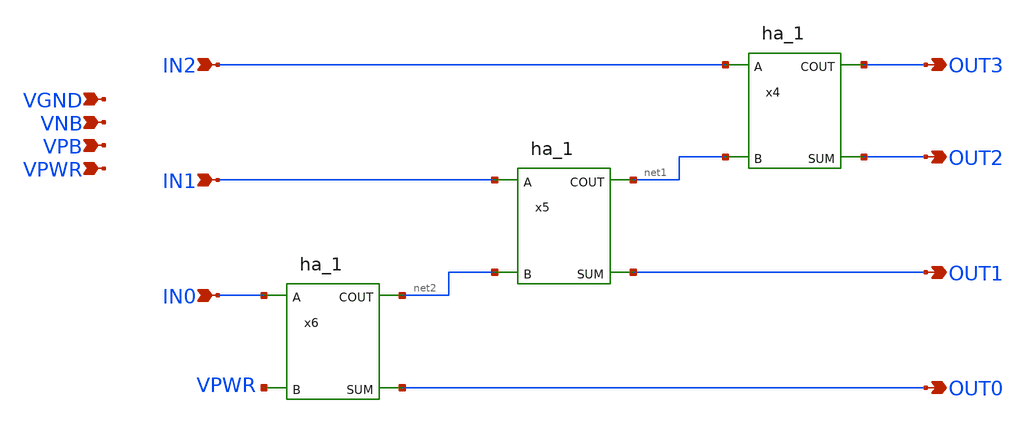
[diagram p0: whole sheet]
** sch_path: project/examples/3bit_counter_busses/3bit_incrementor.sch
**.subckt 3bit_incrementor VGND VNB VPB VPWR IN0 IN1 IN2 OUT0 OUT1 OUT2 OUT3
*.ipin VGND
*.ipin VNB
*.ipin VPB
*.ipin VPWR
*.ipin IN0
*.ipin IN1
*.ipin IN2
*.opin OUT0
*.opin OUT1
*.opin OUT2
*.opin OUT3
x4 IN2 net1 VGND VNB VPB VPWR OUT3 OUT2 sky130_fd_sc_hd__ha_1
x5 IN1 net2 VGND VNB VPB VPWR net1 OUT1 sky130_fd_sc_hd__ha_1
x6 IN0 VPWR VGND VNB VPB VPWR net2 OUT0 sky130_fd_sc_hd__ha_1
**.ends
.end
